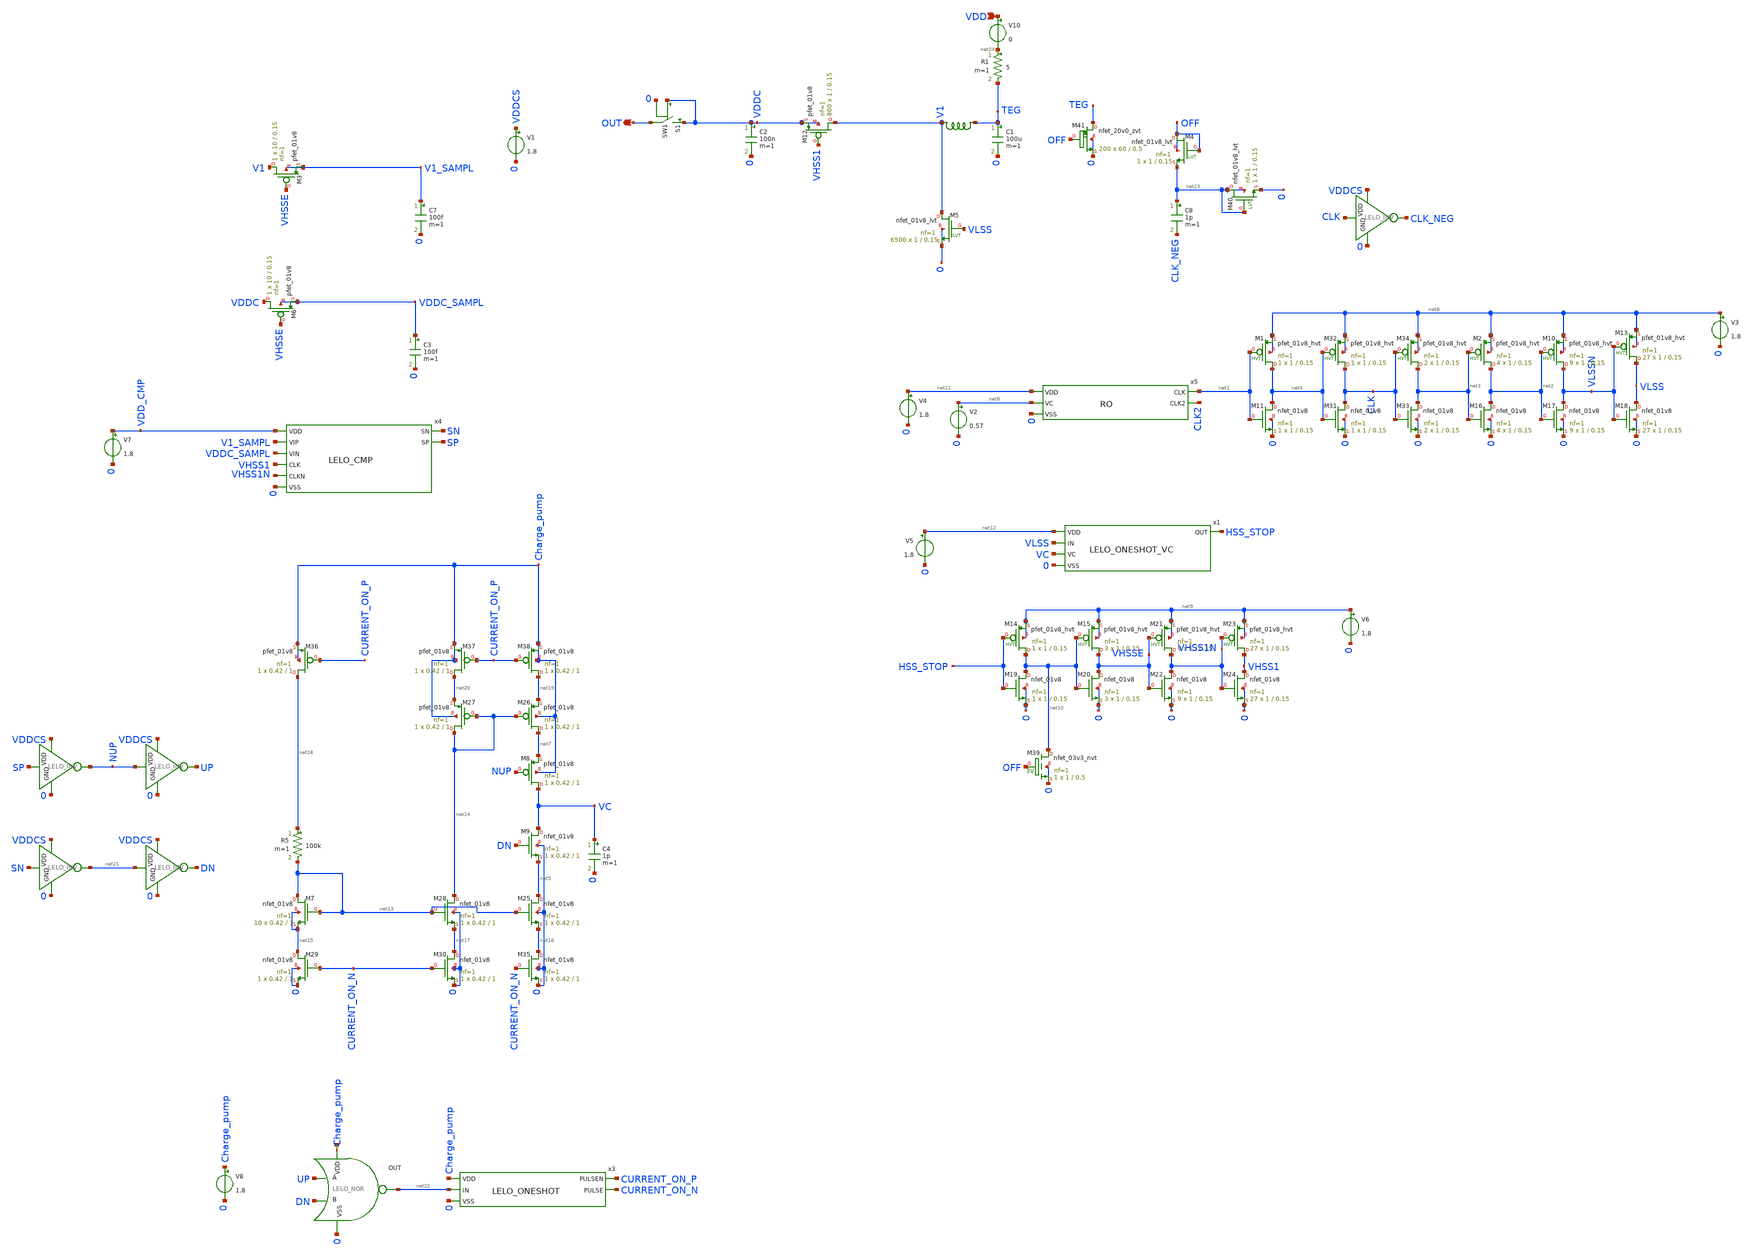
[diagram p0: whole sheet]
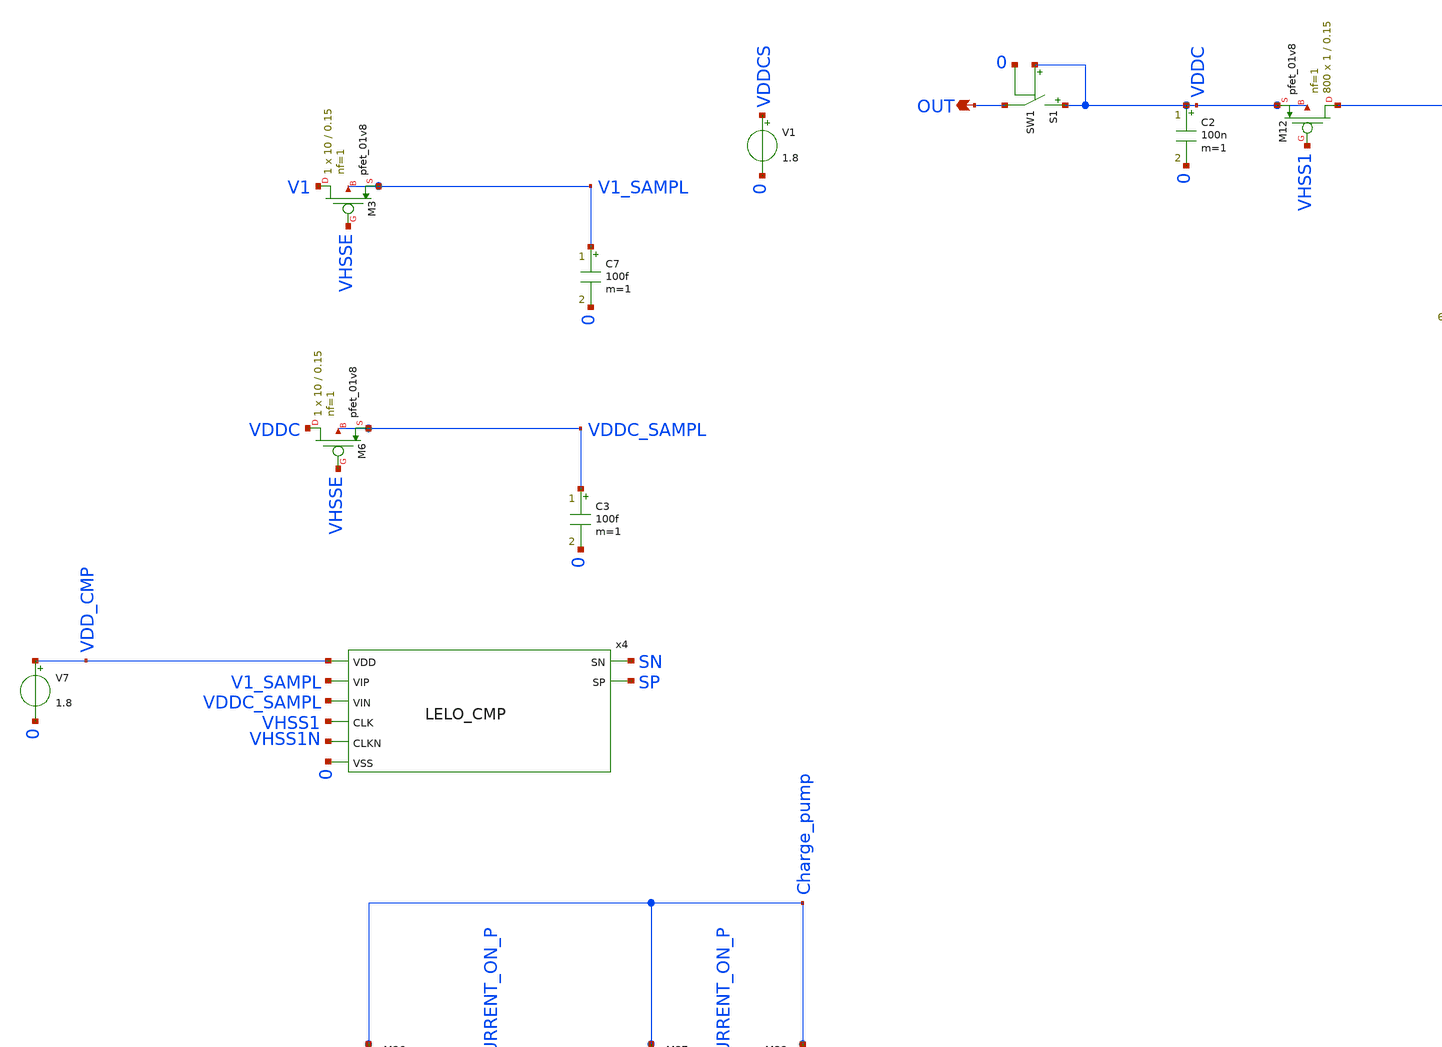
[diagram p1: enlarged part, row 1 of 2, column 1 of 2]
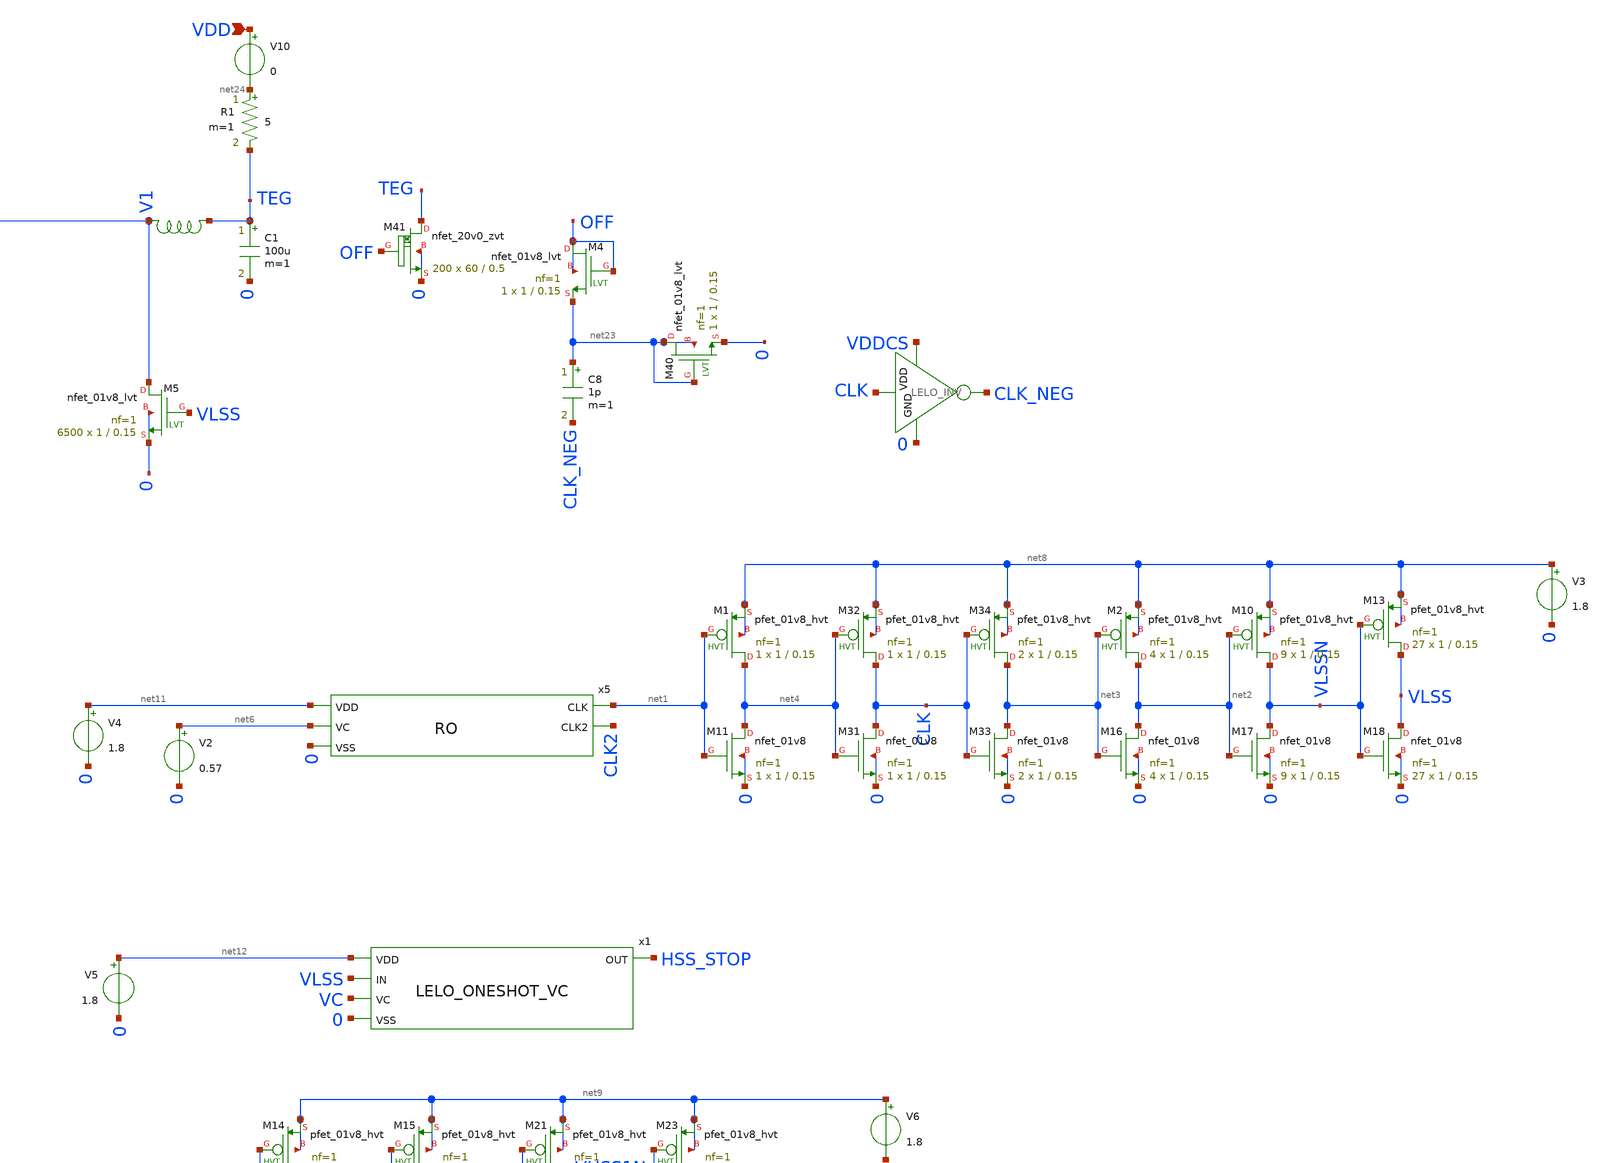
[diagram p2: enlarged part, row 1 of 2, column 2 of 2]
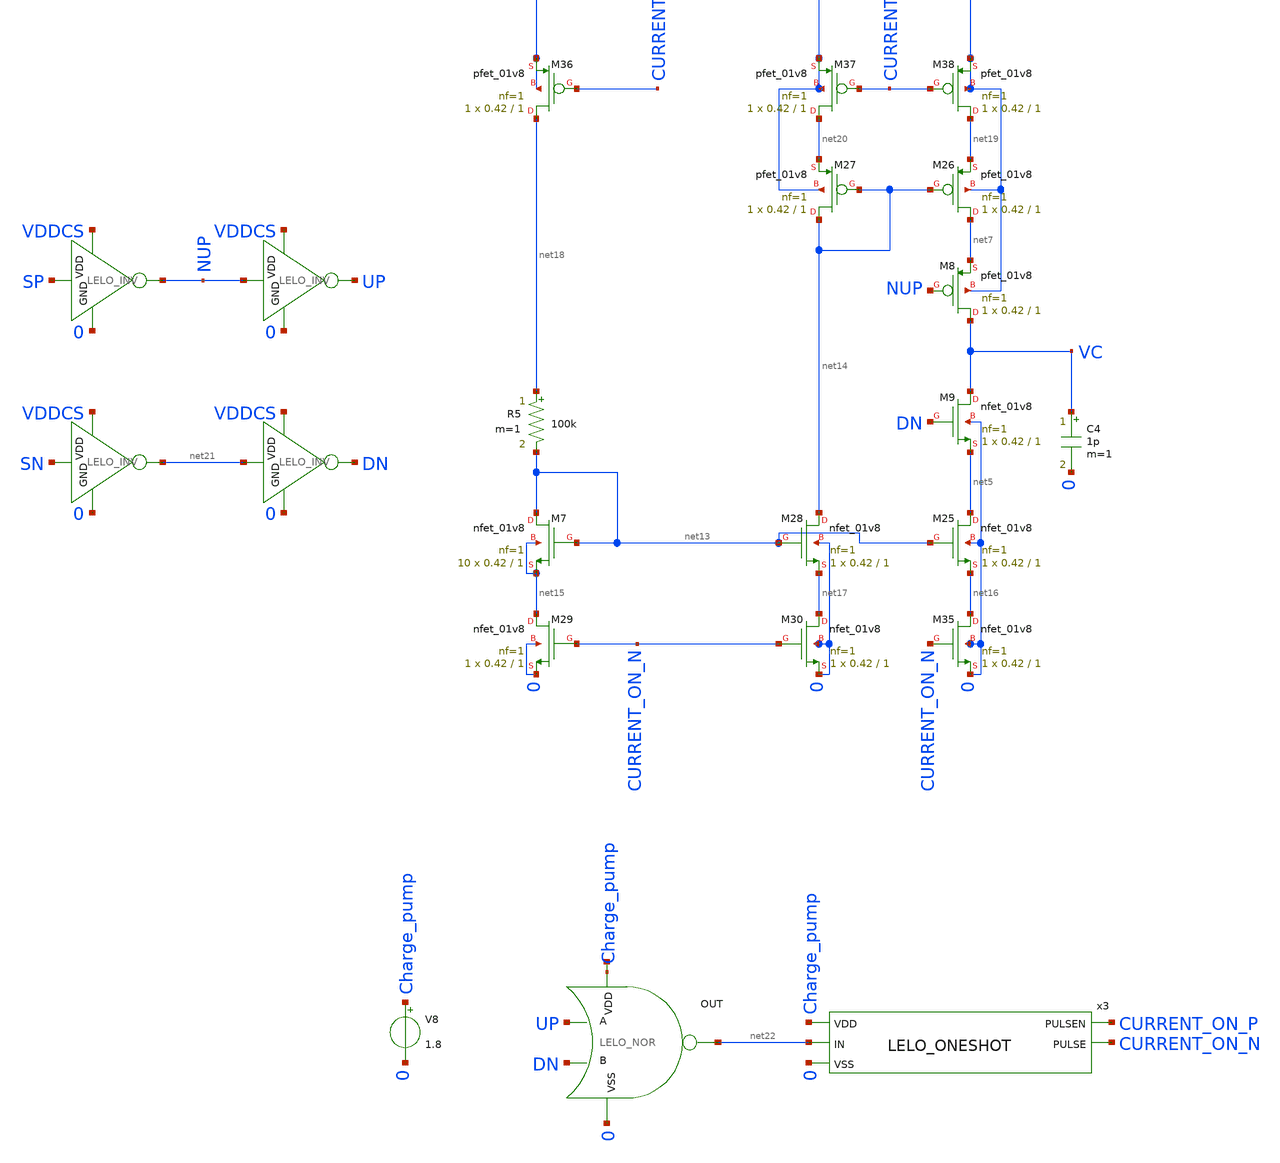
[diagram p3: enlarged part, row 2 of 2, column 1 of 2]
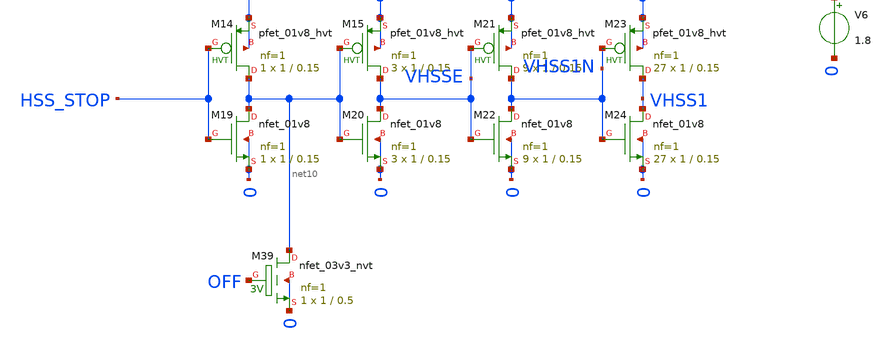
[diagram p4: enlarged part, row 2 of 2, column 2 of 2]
** sch_path: design/LELO_SVOD_SKY130A/LELO_BOOST_STEADY_STATE_TURN.sch
**.subckt LELO_BOOST_STEADY_STATE_TURN VDD OUT
*.ipin VDD
*.opin OUT
R1 net24 TEG 5 m=1
C7 V1_SAMPL 0 100f m=1
x5 net1 CLK2 net11 net6 0 RO
XM12 V1 VHSS1 VDDC VDDC sky130_fd_pr__pfet_01v8 L=0.15 W=1 nf=1 ad='int((1 + 1)/2) * 1 / 1 * 0.29' as='int((1 + 2)/2) * 1 / 1 * 0.29'
+ pd='2*int((1 + 1)/2) * (1 / 1 + 0.29)' ps='2*int((1 + 2)/2) * (1 / 1 + 0.29)' nrd='0.29 / 1 ' nrs='0.29 / 1 '
+ sa=0 sb=0 sd=0 mult=800 m=800
C1 TEG 0 100u m=1
XM5 V1 VLSS 0 0 sky130_fd_pr__nfet_01v8_lvt L=0.15 W=1 nf=1 ad='int((1 + 1)/2) * 1 / 1 * 0.29' as='int((1 + 2)/2) * 1 / 1 * 0.29'
+ pd='2*int((1 + 1)/2) * (1 / 1 + 0.29)' ps='2*int((1 + 2)/2) * (1 / 1 + 0.29)' nrd='0.29 / 1 ' nrs='0.29 / 1 '
+ sa=0 sb=0 sd=0 mult=6500 m=6500
C2 VDDC 0 100n m=1
V1 VDDCS 0 1.8
x4 SN SP VDD_CMP V1_SAMPL VDDC_SAMPL VHSS1 VHSS1N 0 LELO_CMP
XM3 V1 VHSSE V1_SAMPL V1_SAMPL sky130_fd_pr__pfet_01v8 L=0.15 W=10 nf=1 ad='int((1 + 1)/2) * 10 / 1 * 0.29'
+ as='int((1 + 2)/2) * 10 / 1 * 0.29' pd='2*int((1 + 1)/2) * (10 / 1 + 0.29)' ps='2*int((1 + 2)/2) * (10 / 1 + 0.29)'
+ nrd='0.29 / 10 ' nrs='0.29 / 10 ' sa=0 sb=0 sd=0 mult=1 m=1
C3 VDDC_SAMPL 0 100f m=1
XM6 VDDC VHSSE VDDC_SAMPL VDDC_SAMPL sky130_fd_pr__pfet_01v8 L=0.15 W=10 nf=1 ad='int((1 + 1)/2) * 10 / 1 * 0.29'
+ as='int((1 + 2)/2) * 10 / 1 * 0.29' pd='2*int((1 + 1)/2) * (10 / 1 + 0.29)' ps='2*int((1 + 2)/2) * (10 / 1 + 0.29)'
+ nrd='0.29 / 10 ' nrs='0.29 / 10 ' sa=0 sb=0 sd=0 mult=1 m=1
C4 VC 0 1p m=1
XM8 VC NUP net7 Charge_pump sky130_fd_pr__pfet_01v8 L=1 W=0.42 nf=1 ad='int((1 + 1)/2) * 0.42 / 1 * 0.29'
+ as='int((1 + 2)/2) * 0.42 / 1 * 0.29' pd='2*int((1 + 1)/2) * (0.42 / 1 + 0.29)' ps='2*int((1 + 2)/2) * (0.42 / 1 + 0.29)'
+ nrd='0.29 / 0.42 ' nrs='0.29 / 0.42 ' sa=0 sb=0 sd=0 mult=1 m=1
XM9 VC DN net5 0 sky130_fd_pr__nfet_01v8 L=1 W=0.42 nf=1 ad='int((1 + 1)/2) * 0.42 / 1 * 0.29' as='int((1 + 2)/2) * 0.42 / 1 * 0.29'
+ pd='2*int((1 + 1)/2) * (0.42 / 1 + 0.29)' ps='2*int((1 + 2)/2) * (0.42 / 1 + 0.29)' nrd='0.29 / 0.42 '
+ nrs='0.29 / 0.42 ' sa=0 sb=0 sd=0 mult=1 m=1
V2 net6 0 0.57
XM11 net4 net1 0 0 sky130_fd_pr__nfet_01v8 L=0.15 W=1 nf=1 ad='int((1 + 1)/2) * 1 / 1 * 0.29' as='int((1 + 2)/2) * 1 / 1 * 0.29'
+ pd='2*int((1 + 1)/2) * (1 / 1 + 0.29)' ps='2*int((1 + 2)/2) * (1 / 1 + 0.29)' nrd='0.29 / 1 ' nrs='0.29 / 1 '
+ sa=0 sb=0 sd=0 mult=1 m=1
XM16 net2 net3 0 0 sky130_fd_pr__nfet_01v8 L=0.15 W=1 nf=1 ad='int((1 + 1)/2) * 1 / 1 * 0.29' as='int((1 + 2)/2) * 1 / 1 * 0.29'
+ pd='2*int((1 + 1)/2) * (1 / 1 + 0.29)' ps='2*int((1 + 2)/2) * (1 / 1 + 0.29)' nrd='0.29 / 1 ' nrs='0.29 / 1 '
+ sa=0 sb=0 sd=0 mult=4 m=4
XM17 VLSSN net2 0 0 sky130_fd_pr__nfet_01v8 L=0.15 W=1 nf=1 ad='int((1 + 1)/2) * 1 / 1 * 0.29' as='int((1 + 2)/2) * 1 / 1 * 0.29'
+ pd='2*int((1 + 1)/2) * (1 / 1 + 0.29)' ps='2*int((1 + 2)/2) * (1 / 1 + 0.29)' nrd='0.29 / 1 ' nrs='0.29 / 1 '
+ sa=0 sb=0 sd=0 mult=9 m=9
XM18 VLSS VLSSN 0 0 sky130_fd_pr__nfet_01v8 L=0.15 W=1 nf=1 ad='int((1 + 1)/2) * 1 / 1 * 0.29' as='int((1 + 2)/2) * 1 / 1 * 0.29'
+ pd='2*int((1 + 1)/2) * (1 / 1 + 0.29)' ps='2*int((1 + 2)/2) * (1 / 1 + 0.29)' nrd='0.29 / 1 ' nrs='0.29 / 1 '
+ sa=0 sb=0 sd=0 mult=27 m=27
XM19 net10 HSS_STOP 0 0 sky130_fd_pr__nfet_01v8 L=0.15 W=1 nf=1 ad='int((1 + 1)/2) * 1 / 1 * 0.29' as='int((1 + 2)/2) * 1 / 1 * 0.29'
+ pd='2*int((1 + 1)/2) * (1 / 1 + 0.29)' ps='2*int((1 + 2)/2) * (1 / 1 + 0.29)' nrd='0.29 / 1 ' nrs='0.29 / 1 '
+ sa=0 sb=0 sd=0 mult=1 m=1
XM20 VHSSE net10 0 0 sky130_fd_pr__nfet_01v8 L=0.15 W=1 nf=1 ad='int((1 + 1)/2) * 1 / 1 * 0.29' as='int((1 + 2)/2) * 1 / 1 * 0.29'
+ pd='2*int((1 + 1)/2) * (1 / 1 + 0.29)' ps='2*int((1 + 2)/2) * (1 / 1 + 0.29)' nrd='0.29 / 1 ' nrs='0.29 / 1 '
+ sa=0 sb=0 sd=0 mult=3 m=3
XM22 VHSS1N VHSSE 0 0 sky130_fd_pr__nfet_01v8 L=0.15 W=1 nf=1 ad='int((1 + 1)/2) * 1 / 1 * 0.29' as='int((1 + 2)/2) * 1 / 1 * 0.29'
+ pd='2*int((1 + 1)/2) * (1 / 1 + 0.29)' ps='2*int((1 + 2)/2) * (1 / 1 + 0.29)' nrd='0.29 / 1 ' nrs='0.29 / 1 '
+ sa=0 sb=0 sd=0 mult=9 m=9
XM24 VHSS1 VHSS1N 0 0 sky130_fd_pr__nfet_01v8 L=0.15 W=1 nf=1 ad='int((1 + 1)/2) * 1 / 1 * 0.29' as='int((1 + 2)/2) * 1 / 1 * 0.29'
+ pd='2*int((1 + 1)/2) * (1 / 1 + 0.29)' ps='2*int((1 + 2)/2) * (1 / 1 + 0.29)' nrd='0.29 / 1 ' nrs='0.29 / 1 '
+ sa=0 sb=0 sd=0 mult=27 m=27
XM1 net4 net1 net8 net8 sky130_fd_pr__pfet_01v8_hvt L=0.15 W=1 nf=1 ad='int((1 + 1)/2) * 1 / 1 * 0.29'
+ as='int((1 + 2)/2) * 1 / 1 * 0.29' pd='2*int((1 + 1)/2) * (1 / 1 + 0.29)' ps='2*int((1 + 2)/2) * (1 / 1 + 0.29)'
+ nrd='0.29 / 1 ' nrs='0.29 / 1 ' sa=0 sb=0 sd=0 mult=1 m=1
XM2 net2 net3 net8 net8 sky130_fd_pr__pfet_01v8_hvt L=0.15 W=1 nf=1 ad='int((1 + 1)/2) * 1 / 1 * 0.29'
+ as='int((1 + 2)/2) * 1 / 1 * 0.29' pd='2*int((1 + 1)/2) * (1 / 1 + 0.29)' ps='2*int((1 + 2)/2) * (1 / 1 + 0.29)'
+ nrd='0.29 / 1 ' nrs='0.29 / 1 ' sa=0 sb=0 sd=0 mult=4 m=4
XM10 VLSSN net2 net8 net8 sky130_fd_pr__pfet_01v8_hvt L=0.15 W=1 nf=1 ad='int((1 + 1)/2) * 1 / 1 * 0.29'
+ as='int((1 + 2)/2) * 1 / 1 * 0.29' pd='2*int((1 + 1)/2) * (1 / 1 + 0.29)' ps='2*int((1 + 2)/2) * (1 / 1 + 0.29)'
+ nrd='0.29 / 1 ' nrs='0.29 / 1 ' sa=0 sb=0 sd=0 mult=9 m=9
XM13 VLSS VLSSN net8 net8 sky130_fd_pr__pfet_01v8_hvt L=0.15 W=1 nf=1 ad='int((1 + 1)/2) * 1 / 1 * 0.29'
+ as='int((1 + 2)/2) * 1 / 1 * 0.29' pd='2*int((1 + 1)/2) * (1 / 1 + 0.29)' ps='2*int((1 + 2)/2) * (1 / 1 + 0.29)'
+ nrd='0.29 / 1 ' nrs='0.29 / 1 ' sa=0 sb=0 sd=0 mult=27 m=27
XM14 net10 HSS_STOP net9 net9 sky130_fd_pr__pfet_01v8_hvt L=0.15 W=1 nf=1 ad='int((1 + 1)/2) * 1 / 1 * 0.29'
+ as='int((1 + 2)/2) * 1 / 1 * 0.29' pd='2*int((1 + 1)/2) * (1 / 1 + 0.29)' ps='2*int((1 + 2)/2) * (1 / 1 + 0.29)'
+ nrd='0.29 / 1 ' nrs='0.29 / 1 ' sa=0 sb=0 sd=0 mult=1 m=1
XM15 VHSSE net10 net9 net9 sky130_fd_pr__pfet_01v8_hvt L=0.15 W=1 nf=1 ad='int((1 + 1)/2) * 1 / 1 * 0.29'
+ as='int((1 + 2)/2) * 1 / 1 * 0.29' pd='2*int((1 + 1)/2) * (1 / 1 + 0.29)' ps='2*int((1 + 2)/2) * (1 / 1 + 0.29)'
+ nrd='0.29 / 1 ' nrs='0.29 / 1 ' sa=0 sb=0 sd=0 mult=3 m=3
XM21 VHSS1N VHSSE net9 net9 sky130_fd_pr__pfet_01v8_hvt L=0.15 W=1 nf=1 ad='int((1 + 1)/2) * 1 / 1 * 0.29'
+ as='int((1 + 2)/2) * 1 / 1 * 0.29' pd='2*int((1 + 1)/2) * (1 / 1 + 0.29)' ps='2*int((1 + 2)/2) * (1 / 1 + 0.29)'
+ nrd='0.29 / 1 ' nrs='0.29 / 1 ' sa=0 sb=0 sd=0 mult=9 m=9
XM23 VHSS1 VHSS1N net9 net9 sky130_fd_pr__pfet_01v8_hvt L=0.15 W=1 nf=1 ad='int((1 + 1)/2) * 1 / 1 * 0.29'
+ as='int((1 + 2)/2) * 1 / 1 * 0.29' pd='2*int((1 + 1)/2) * (1 / 1 + 0.29)' ps='2*int((1 + 2)/2) * (1 / 1 + 0.29)'
+ nrd='0.29 / 1 ' nrs='0.29 / 1 ' sa=0 sb=0 sd=0 mult=27 m=27
V4 net11 0 1.8
V3 net8 0 1.8
V5 net12 0 1.8
V6 net9 0 1.8
V7 VDD_CMP 0 1.8
XM31 CLK net4 0 0 sky130_fd_pr__nfet_01v8 L=0.15 W=1 nf=1 ad='int((1 + 1)/2) * 1 / 1 * 0.29' as='int((1 + 2)/2) * 1 / 1 * 0.29'
+ pd='2*int((1 + 1)/2) * (1 / 1 + 0.29)' ps='2*int((1 + 2)/2) * (1 / 1 + 0.29)' nrd='0.29 / 1 ' nrs='0.29 / 1 '
+ sa=0 sb=0 sd=0 mult=1 m=1
XM32 CLK net4 net8 net8 sky130_fd_pr__pfet_01v8_hvt L=0.15 W=1 nf=1 ad='int((1 + 1)/2) * 1 / 1 * 0.29'
+ as='int((1 + 2)/2) * 1 / 1 * 0.29' pd='2*int((1 + 1)/2) * (1 / 1 + 0.29)' ps='2*int((1 + 2)/2) * (1 / 1 + 0.29)'
+ nrd='0.29 / 1 ' nrs='0.29 / 1 ' sa=0 sb=0 sd=0 mult=1 m=1
XM33 net3 CLK 0 0 sky130_fd_pr__nfet_01v8 L=0.15 W=1 nf=1 ad='int((1 + 1)/2) * 1 / 1 * 0.29' as='int((1 + 2)/2) * 1 / 1 * 0.29'
+ pd='2*int((1 + 1)/2) * (1 / 1 + 0.29)' ps='2*int((1 + 2)/2) * (1 / 1 + 0.29)' nrd='0.29 / 1 ' nrs='0.29 / 1 '
+ sa=0 sb=0 sd=0 mult=2 m=2
XM34 net3 CLK net8 net8 sky130_fd_pr__pfet_01v8_hvt L=0.15 W=1 nf=1 ad='int((1 + 1)/2) * 1 / 1 * 0.29'
+ as='int((1 + 2)/2) * 1 / 1 * 0.29' pd='2*int((1 + 1)/2) * (1 / 1 + 0.29)' ps='2*int((1 + 2)/2) * (1 / 1 + 0.29)'
+ nrd='0.29 / 1 ' nrs='0.29 / 1 ' sa=0 sb=0 sd=0 mult=2 m=2
x7 TEG V1 XGL6030-822_sat
x10 VDDCS SP NUP 0 LELO_INV
R5 net18 net13 100k m=1
XM7 net13 net13 net15 net15 sky130_fd_pr__nfet_01v8 L=1 W=0.42 nf=1 ad='int((1 + 1)/2) * 0.42 / 1 * 0.29'
+ as='int((1 + 2)/2) * 0.42 / 1 * 0.29' pd='2*int((1 + 1)/2) * (0.42 / 1 + 0.29)' ps='2*int((1 + 2)/2) * (0.42 / 1 + 0.29)'
+ nrd='0.29 / 0.42 ' nrs='0.29 / 0.42 ' sa=0 sb=0 sd=0 mult=10 m=10
XM25 net5 net13 net16 0 sky130_fd_pr__nfet_01v8 L=1 W=0.42 nf=1 ad='int((1 + 1)/2) * 0.42 / 1 * 0.29'
+ as='int((1 + 2)/2) * 0.42 / 1 * 0.29' pd='2*int((1 + 1)/2) * (0.42 / 1 + 0.29)' ps='2*int((1 + 2)/2) * (0.42 / 1 + 0.29)'
+ nrd='0.29 / 0.42 ' nrs='0.29 / 0.42 ' sa=0 sb=0 sd=0 mult=1 m=1
XM26 net7 net14 net19 Charge_pump sky130_fd_pr__pfet_01v8 L=1 W=0.42 nf=1 ad='int((1 + 1)/2) * 0.42 / 1 * 0.29'
+ as='int((1 + 2)/2) * 0.42 / 1 * 0.29' pd='2*int((1 + 1)/2) * (0.42 / 1 + 0.29)' ps='2*int((1 + 2)/2) * (0.42 / 1 + 0.29)'
+ nrd='0.29 / 0.42 ' nrs='0.29 / 0.42 ' sa=0 sb=0 sd=0 mult=1 m=1
XM27 net14 net14 net20 Charge_pump sky130_fd_pr__pfet_01v8 L=1 W=0.42 nf=1 ad='int((1 + 1)/2) * 0.42 / 1 * 0.29'
+ as='int((1 + 2)/2) * 0.42 / 1 * 0.29' pd='2*int((1 + 1)/2) * (0.42 / 1 + 0.29)' ps='2*int((1 + 2)/2) * (0.42 / 1 + 0.29)'
+ nrd='0.29 / 0.42 ' nrs='0.29 / 0.42 ' sa=0 sb=0 sd=0 mult=1 m=1
XM28 net14 net13 net17 0 sky130_fd_pr__nfet_01v8 L=1 W=0.42 nf=1 ad='int((1 + 1)/2) * 0.42 / 1 * 0.29'
+ as='int((1 + 2)/2) * 0.42 / 1 * 0.29' pd='2*int((1 + 1)/2) * (0.42 / 1 + 0.29)' ps='2*int((1 + 2)/2) * (0.42 / 1 + 0.29)'
+ nrd='0.29 / 0.42 ' nrs='0.29 / 0.42 ' sa=0 sb=0 sd=0 mult=1 m=1
XM29 net15 CURRENT_ON_N 0 0 sky130_fd_pr__nfet_01v8 L=1 W=0.42 nf=1 ad='int((1 + 1)/2) * 0.42 / 1 * 0.29'
+ as='int((1 + 2)/2) * 0.42 / 1 * 0.29' pd='2*int((1 + 1)/2) * (0.42 / 1 + 0.29)' ps='2*int((1 + 2)/2) * (0.42 / 1 + 0.29)'
+ nrd='0.29 / 0.42 ' nrs='0.29 / 0.42 ' sa=0 sb=0 sd=0 mult=1 m=1
XM30 net17 CURRENT_ON_N 0 0 sky130_fd_pr__nfet_01v8 L=1 W=0.42 nf=1 ad='int((1 + 1)/2) * 0.42 / 1 * 0.29'
+ as='int((1 + 2)/2) * 0.42 / 1 * 0.29' pd='2*int((1 + 1)/2) * (0.42 / 1 + 0.29)' ps='2*int((1 + 2)/2) * (0.42 / 1 + 0.29)'
+ nrd='0.29 / 0.42 ' nrs='0.29 / 0.42 ' sa=0 sb=0 sd=0 mult=1 m=1
XM35 net16 CURRENT_ON_N 0 0 sky130_fd_pr__nfet_01v8 L=1 W=0.42 nf=1 ad='int((1 + 1)/2) * 0.42 / 1 * 0.29'
+ as='int((1 + 2)/2) * 0.42 / 1 * 0.29' pd='2*int((1 + 1)/2) * (0.42 / 1 + 0.29)' ps='2*int((1 + 2)/2) * (0.42 / 1 + 0.29)'
+ nrd='0.29 / 0.42 ' nrs='0.29 / 0.42 ' sa=0 sb=0 sd=0 mult=1 m=1
XM36 net18 CURRENT_ON_P Charge_pump Charge_pump sky130_fd_pr__pfet_01v8 L=1 W=0.42 nf=1 ad='int((1 + 1)/2) * 0.42 / 1 * 0.29'
+ as='int((1 + 2)/2) * 0.42 / 1 * 0.29' pd='2*int((1 + 1)/2) * (0.42 / 1 + 0.29)' ps='2*int((1 + 2)/2) * (0.42 / 1 + 0.29)'
+ nrd='0.29 / 0.42 ' nrs='0.29 / 0.42 ' sa=0 sb=0 sd=0 mult=1 m=1
XM37 net20 CURRENT_ON_P Charge_pump Charge_pump sky130_fd_pr__pfet_01v8 L=1 W=0.42 nf=1 ad='int((1 + 1)/2) * 0.42 / 1 * 0.29'
+ as='int((1 + 2)/2) * 0.42 / 1 * 0.29' pd='2*int((1 + 1)/2) * (0.42 / 1 + 0.29)' ps='2*int((1 + 2)/2) * (0.42 / 1 + 0.29)'
+ nrd='0.29 / 0.42 ' nrs='0.29 / 0.42 ' sa=0 sb=0 sd=0 mult=1 m=1
XM38 net19 CURRENT_ON_P Charge_pump Charge_pump sky130_fd_pr__pfet_01v8 L=1 W=0.42 nf=1 ad='int((1 + 1)/2) * 0.42 / 1 * 0.29'
+ as='int((1 + 2)/2) * 0.42 / 1 * 0.29' pd='2*int((1 + 1)/2) * (0.42 / 1 + 0.29)' ps='2*int((1 + 2)/2) * (0.42 / 1 + 0.29)'
+ nrd='0.29 / 0.42 ' nrs='0.29 / 0.42 ' sa=0 sb=0 sd=0 mult=1 m=1
V8 Charge_pump 0 1.8
x11 VDDCS SN net21 0 LELO_INV
x14 VDDCS net21 DN 0 LELO_INV
x17 VDDCS NUP UP 0 LELO_INV
x1 net12 VLSS VC HSS_STOP 0 LELO_ONESHOT_VC
x2 net25 net22 UP DN 0 LELO_NOR
x3 Charge_pump net22 0 CURRENT_ON_P CURRENT_ON_N LELO_ONESHOT
C8 net23 CLK_NEG 1p m=1
XM4 OFF OFF net23 OFF sky130_fd_pr__nfet_01v8_lvt L=0.15 W=1 nf=1 ad='int((1 + 1)/2) * 1 / 1 * 0.29'
+ as='int((1 + 2)/2) * 1 / 1 * 0.29' pd='2*int((1 + 1)/2) * (1 / 1 + 0.29)' ps='2*int((1 + 2)/2) * (1 / 1 + 0.29)'
+ nrd='0.29 / 1 ' nrs='0.29 / 1 ' sa=0 sb=0 sd=0 mult=1 m=1
x8 VDDCS CLK CLK_NEG 0 LELO_INV
XM39 net10 OFF 0 0 sky130_fd_pr__nfet_03v3_nvt L=0.5 W=1 nf=1 ad='int((1 + 1)/2) * 1 / 1 * 0.29' as='int((1 + 2)/2) * 1 / 1 * 0.29'
+ pd='2*int((1 + 1)/2) * (1 / 1 + 0.29)' ps='2*int((1 + 2)/2) * (1 / 1 + 0.29)' nrd='0.29 / 1 ' nrs='0.29 / 1 '
+ sa=0 sb=0 sd=0 mult=1 m=1
XM40 net23 net23 0 net23 sky130_fd_pr__nfet_01v8_lvt L=0.15 W=1 nf=1 ad='int((1 + 1)/2) * 1 / 1 * 0.29'
+ as='int((1 + 2)/2) * 1 / 1 * 0.29' pd='2*int((1 + 1)/2) * (1 / 1 + 0.29)' ps='2*int((1 + 2)/2) * (1 / 1 + 0.29)'
+ nrd='0.29 / 1 ' nrs='0.29 / 1 ' sa=0 sb=0 sd=0 mult=1 m=1
XM41 TEG OFF 0 0 sky130_fd_pr__nfet_20v0_zvt W=60 L=0.5 m=200
S1 VDDC OUT VDDC 0 SW1
V10 VDD net24 0
**.ends
**** begin user architecture code
.MODEL SW1 SW   VT=1.8 VH=0.0001  RON=0.01 ROFF=10G
**** end user architecture code
.end
